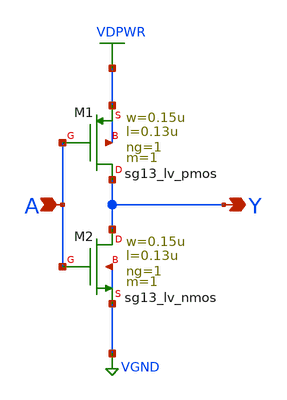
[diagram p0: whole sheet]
** sch_path: xschem/skullfet_inverter.sch
**.subckt skullfet_inverter A Y
*.ipin A
*.opin Y
XM1 Y A VDPWR VDPWR sg13_lv_pmos w=0.15u l=0.13u ng=1 m=1 mm_ok=1
XM2 Y A VGND VGND sg13_lv_nmos w=0.15u l=0.13u ng=1 m=1 mm_ok=1
**.ends
.GLOBAL VGND
.GLOBAL VDPWR
.end
